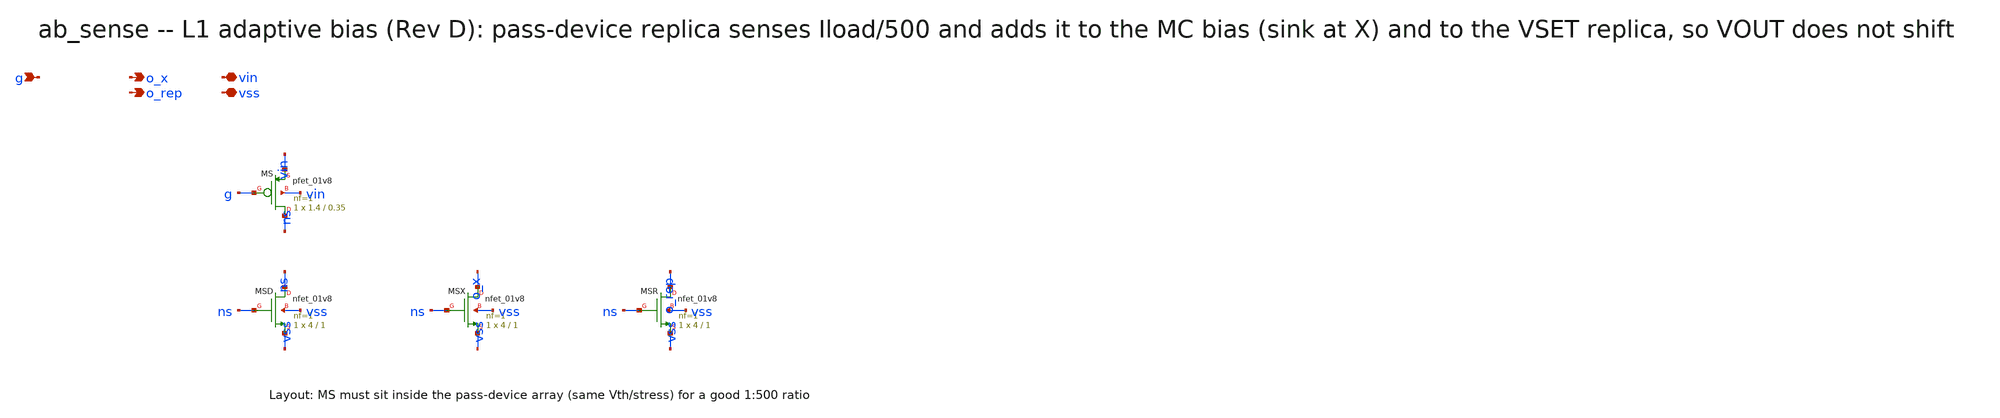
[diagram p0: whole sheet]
** sch_path: xschem/onetops/ab_sense.sch
**.subckt ab_sense g o_x o_rep vin vss
*.ipin g
*.opin o_x
*.opin o_rep
*.iopin vin
*.iopin vss
XMS ns g vin vin sky130_fd_pr__pfet_01v8 L=0.35 W=1.4 nf=1 ad='int((1 + 1)/2) * 1.4 / 1 * 0.29' as='int((1 + 2)/2) * 1.4 / 1 * 0.29'
+ pd='2*int((1 + 1)/2) * (1.4 / 1 + 0.29)' ps='2*int((1 + 2)/2) * (1.4 / 1 + 0.29)' nrd='0.29 / 1.4 ' nrs='0.29 / 1.4 '
+ sa=0 sb=0 sd=0 mult=1 m=1
XMSD ns ns vss vss sky130_fd_pr__nfet_01v8 L=1 W=4 nf=1 ad='int((1 + 1)/2) * 4 / 1 * 0.29' as='int((1 + 2)/2) * 4 / 1 * 0.29'
+ pd='2*int((1 + 1)/2) * (4 / 1 + 0.29)' ps='2*int((1 + 2)/2) * (4 / 1 + 0.29)' nrd='0.29 / 4 ' nrs='0.29 / 4 '
+ sa=0 sb=0 sd=0 mult=1 m=1
XMSX o_x ns vss vss sky130_fd_pr__nfet_01v8 L=1 W=4 nf=1 ad='int((1 + 1)/2) * 4 / 1 * 0.29' as='int((1 + 2)/2) * 4 / 1 * 0.29'
+ pd='2*int((1 + 1)/2) * (4 / 1 + 0.29)' ps='2*int((1 + 2)/2) * (4 / 1 + 0.29)' nrd='0.29 / 4 ' nrs='0.29 / 4 '
+ sa=0 sb=0 sd=0 mult=1 m=1
XMSR o_rep ns vss vss sky130_fd_pr__nfet_01v8 L=1 W=4 nf=1 ad='int((1 + 1)/2) * 4 / 1 * 0.29' as='int((1 + 2)/2) * 4 / 1 * 0.29'
+ pd='2*int((1 + 1)/2) * (4 / 1 + 0.29)' ps='2*int((1 + 2)/2) * (4 / 1 + 0.29)' nrd='0.29 / 4 ' nrs='0.29 / 4 '
+ sa=0 sb=0 sd=0 mult=1 m=1
**.ends
.end
